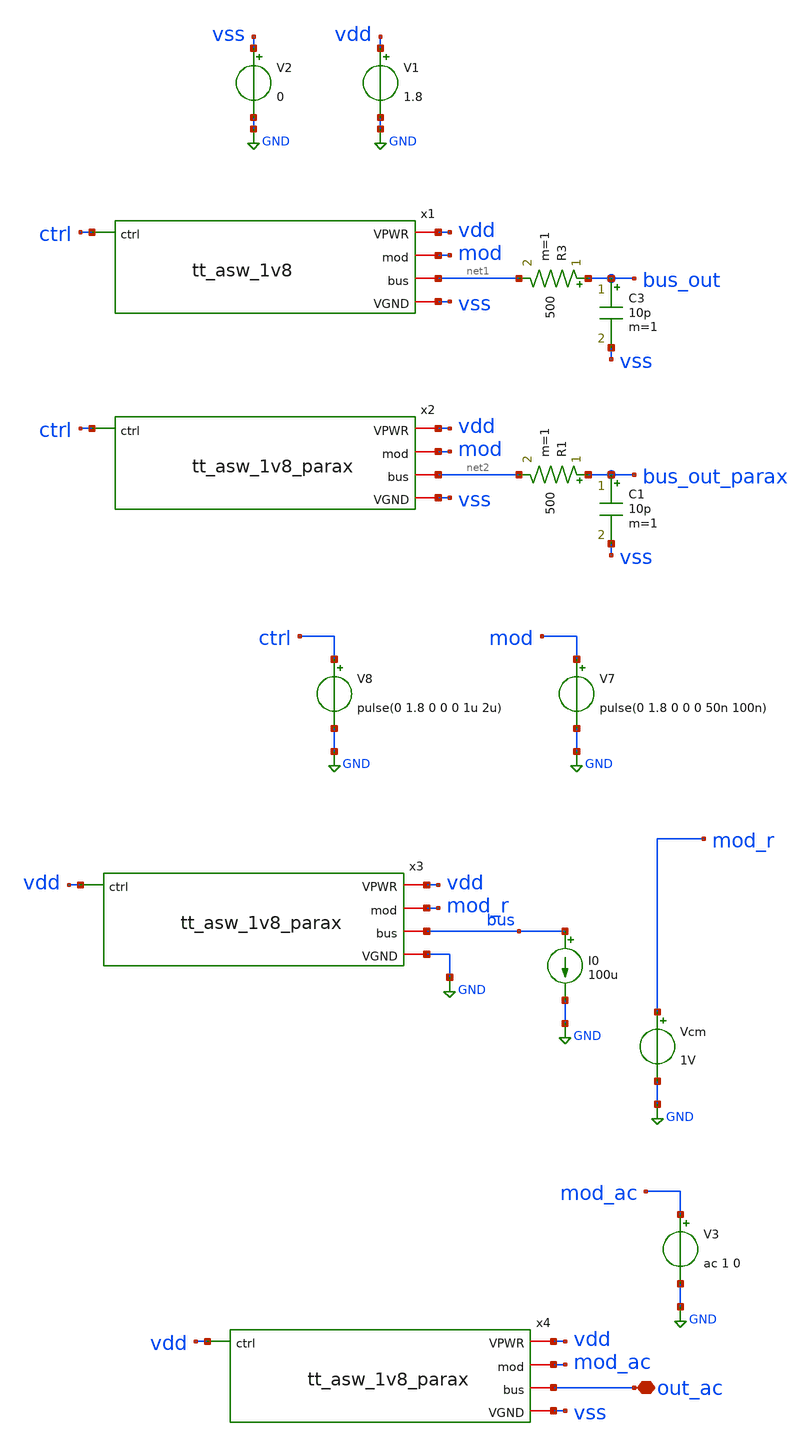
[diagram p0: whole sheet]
** sch_path: xschem/testbench.sch
**.subckt testbench out_ac
*.iopin out_ac
x1 vdd ctrl mod net1 vss tt_asw_1v8
V1 vdd GND 1.8
R3 bus_out net1 500 m=1
C3 bus_out vss 10p m=1
V2 vss GND 0
V7 mod GND pulse(0 1.8 0 0 0 50n 100n)
V8 ctrl GND pulse(0 1.8 0 0 0 1u 2u)
x2 vdd ctrl mod net2 vss tt_asw_1v8_parax
R1 bus_out_parax net2 500 m=1
C1 bus_out_parax vss 10p m=1
x3 vdd vdd mod_r bus GND tt_asw_1v8_parax
Vcm mod_r GND 1V
I0 bus GND 100u
V3 mod_ac GND ac 1 0
x4 vdd vdd mod_ac out_ac vss tt_asw_1v8_parax
**** begin user architecture code

** opencircuitdesign pdks install
.lib $::SKYWATER_MODELS/sky130.lib.spice tt
.include $::SKYWATER_STDCELLS/sky130_fd_sc_hd.spice





.param mc_mm_switch=0
.control
save all
tran 500p 2u uic
write testbench.raw
reset
save all
dc Vcm 0 1.8 0.01
remzerovec
write testbench_dc.raw

ac dec 10 1 200e6
remzerovec
write testbench_ac.raw

*quit 0
.endc
.end


**** end user architecture code
**.ends

* expanding   symbol:  tt_asw_1v8.sym # of pins=5
** sym_path: xschem/tt_asw_1v8.sym
** sch_path: xschem/tt_asw_1v8.sch
.subckt tt_asw_1v8 VPWR ctrl mod bus VGND
*.iopin VPWR
*.iopin VGND
*.iopin mod
*.iopin bus
*.ipin ctrl
XM3 bus tgon mod VGND sky130_fd_pr__nfet_01v8 L=0.15 W=10 nf=4 ad='int((nf+1)/2) * W/nf * 0.29' as='int((nf+2)/2) * W/nf * 0.29'
+ pd='2*int((nf+1)/2) * (W/nf + 0.29)' ps='2*int((nf+2)/2) * (W/nf + 0.29)' nrd='0.29 / W' nrs='0.29 / W'
+ sa=0 sb=0 sd=0 mult=1 m=1
XM4A bus tgon_n mod VPWR sky130_fd_pr__pfet_01v8 L=0.15 W=20 nf=8 ad='int((nf+1)/2) * W/nf * 0.29' as='int((nf+2)/2) * W/nf * 0.29'
+ pd='2*int((nf+1)/2) * (W/nf + 0.29)' ps='2*int((nf+2)/2) * (W/nf + 0.29)' nrd='0.29 / W' nrs='0.29 / W'
+ sa=0 sb=0 sd=0 mult=1 m=1
XM1 tgon tgon_n VGND VGND sky130_fd_pr__nfet_01v8 L=0.15 W=2.5 nf=1 ad='int((nf+1)/2) * W/nf * 0.29'
+ as='int((nf+2)/2) * W/nf * 0.29' pd='2*int((nf+1)/2) * (W/nf + 0.29)' ps='2*int((nf+2)/2) * (W/nf + 0.29)'
+ nrd='0.29 / W' nrs='0.29 / W' sa=0 sb=0 sd=0 mult=1 m=1
XM2 tgon tgon_n VPWR VPWR sky130_fd_pr__pfet_01v8 L=0.15 W=5 nf=2 ad='int((nf+1)/2) * W/nf * 0.29' as='int((nf+2)/2) * W/nf * 0.29'
+ pd='2*int((nf+1)/2) * (W/nf + 0.29)' ps='2*int((nf+2)/2) * (W/nf + 0.29)' nrd='0.29 / W' nrs='0.29 / W'
+ sa=0 sb=0 sd=0 mult=1 m=1
XM5 tgon_n ctrl VGND VGND sky130_fd_pr__nfet_01v8 L=0.15 W=2.5 nf=1 ad='int((nf+1)/2) * W/nf * 0.29'
+ as='int((nf+2)/2) * W/nf * 0.29' pd='2*int((nf+1)/2) * (W/nf + 0.29)' ps='2*int((nf+2)/2) * (W/nf + 0.29)'
+ nrd='0.29 / W' nrs='0.29 / W' sa=0 sb=0 sd=0 mult=1 m=1
XM4 tgon_n ctrl VPWR VPWR sky130_fd_pr__pfet_01v8 L=0.15 W=5 nf=2 ad='int((nf+1)/2) * W/nf * 0.29' as='int((nf+2)/2) * W/nf * 0.29'
+ pd='2*int((nf+1)/2) * (W/nf + 0.29)' ps='2*int((nf+2)/2) * (W/nf + 0.29)' nrd='0.29 / W' nrs='0.29 / W'
+ sa=0 sb=0 sd=0 mult=1 m=1
.ends


* expanding   symbol:  tt_asw_1v8_parax.sym # of pins=5
** sym_path: xschem/tt_asw_1v8.sym
.include [file normalize ../mag/tt_asw_1v8.sim.spice]
.GLOBAL GND
.end
